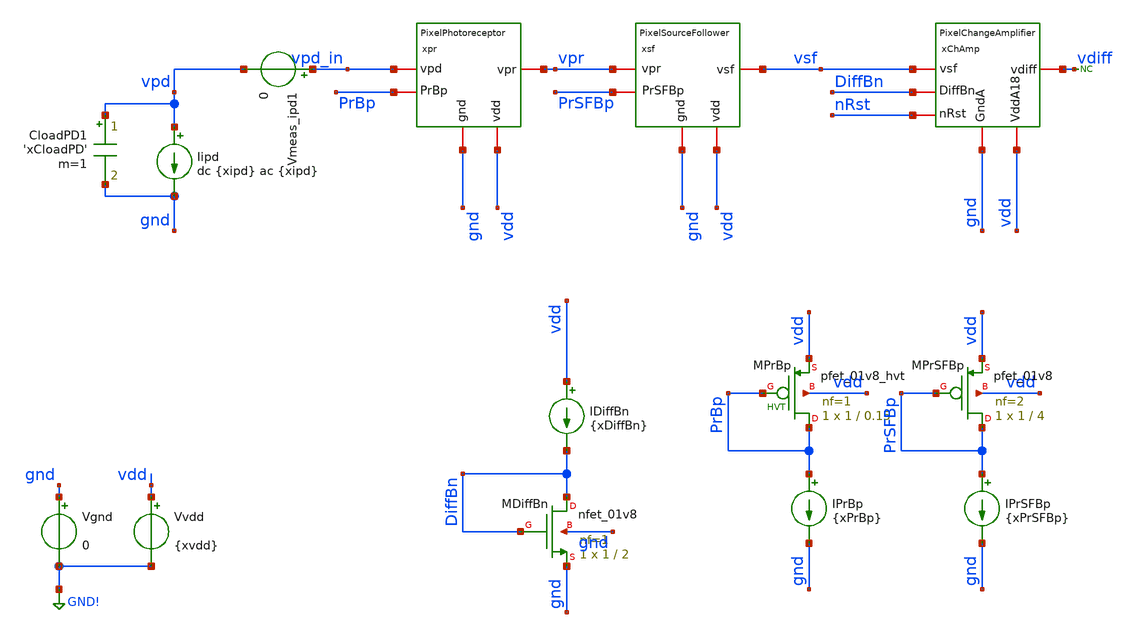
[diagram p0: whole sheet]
** sch_path: analog/klayout/production/final_merge_20260923/testbenches/cace/analog/xschem/tb_PixelGain_ac.sch
**.subckt tb_PixelGain_ac
Vgnd gnd GND! 0
Vvdd vdd GND! {xvdd}
xpr vdd PrBp gnd vpd_in vpr PixelPhotoreceptor
xsf vdd PrSFBp gnd vpr vsf PixelSourceFollower
Iipd vpd gnd dc {xipd} ac {xipd}
CloadPD1 vpd gnd 'xCloadPD' m=1
Vmeas_ipd1 vpd_in vpd 0
xChAmp vdd DiffBn gnd vsf vdiff nRst PixelChangeAmplifier
XMDiffBn DiffBn DiffBn gnd gnd sky130_fd_pr__nfet_01v8 L=2 W=1 nf=1 ad='int((1 + 1)/2) * 1 / 1 * 0.29'
+ as='int((1 + 2)/2) * 1 / 1 * 0.29' pd='2*int((1 + 1)/2) * (1 / 1 + 0.29)' ps='2*int((1 + 2)/2) * (1 / 1 + 0.29)'
+ nrd='0.29 / 1 ' nrs='0.29 / 1 ' sa=0 sb=0 sd=0 mult=1 m=1
IDiffBn vdd DiffBn {xDiffBn}
IPrBp PrBp gnd {xPrBp}
XMPrBp PrBp PrBp vdd vdd sky130_fd_pr__pfet_01v8_hvt L=0.15 W=1 nf=1 ad='int((1 + 1)/2) * 1 / 1 * 0.29'
+ as='int((1 + 2)/2) * 1 / 1 * 0.29' pd='2*int((1 + 1)/2) * (1 / 1 + 0.29)' ps='2*int((1 + 2)/2) * (1 / 1 + 0.29)'
+ nrd='0.29 / 1 ' nrs='0.29 / 1 ' sa=0 sb=0 sd=0 mult=1 m=1
IPrSFBp PrSFBp gnd {xPrSFBp}
XMPrSFBp PrSFBp PrSFBp vdd vdd sky130_fd_pr__pfet_01v8 L=4 W=1 nf=2 ad='int((2 + 1)/2) * 1 / 2 * 0.29'
+ as='int((2 + 2)/2) * 1 / 2 * 0.29' pd='2*int((2 + 1)/2) * (1 / 2 + 0.29)' ps='2*int((2 + 2)/2) * (1 / 2 + 0.29)'
+ nrd='0.29 / 1 ' nrs='0.29 / 1 ' sa=0 sb=0 sd=0 mult=1 m=1
* noconn vdiff
**** begin user architecture code

** opencircuitdesign pdks install
.lib $::SKYWATER_MODELS/sky130.lib.spice tt



.temp 27

.option gmin=1e-16 abstol=1e-15 vntol=1e-9 reltol=1e-4 chgtol=1e-16
.option itl1=500 itl2=200
.option gminsteps=200 srcsteps=200

.param xvdd = 1.8
.param xipd = 1p
.param xPrBp = 10n
.param xPrSFBp = 100p
.param xDiffBn = 5n
.param xCloadPD = 30f

** nRst at vdd for normal operation (Mrst OFF)
VnRst nRst gnd {xvdd}

** Large inductor: DC short (sets OP) but AC open (no effect on freq response)
** Provides DC path for floating cap node xchamp.vd through vdiff
Lbias vdiff xchamp.vd 1000T

.save all

.control
** OP with nRst=vdd, .nodeset guides floating nodes
op
let vd_op = v(xchamp.vd)
let vdiff_op = v(vdiff)
echo
echo '=== OP (nRst=vdd) ==='
echo '    vd    =' $&vd_op 'V'
echo '    vdiff =' $&vdiff_op 'V'
write tb_PixelGain_ac_op.raw

** AC sweep from this operating point
ac dec 50 1m 1G
write tb_PixelGain_ac.raw

echo
echo '=== AC analysis complete, running post-processing ==='
shell python3
+ /home/rpgraca/research/projects/telluride/2025/nic_eventcam/nic2025_openDVS/analog/xschem/process_PixelGain_ac.py tb_PixelGain_ac.raw
.endc


**** end user architecture code
**.ends

* expanding   symbol:  PixelPhotoreceptor.sym # of pins=5
** sym_path: analog/xschem/PixelPhotoreceptor.sym
** sch_path: analog/xschem/PixelPhotoreceptor.sch
.subckt PixelPhotoreceptor vdd PrBp gnd vpd vpr
*.iopin PrBp
*.iopin vdd
*.iopin vpd
*.iopin gnd
*.iopin vpr
XMpd vdd vpr vpd gnd sky130_fd_pr__nfet_01v8 L=0.3 W=0.42 nf=1 ad='int((1 + 1)/2) * 0.42 / 1 * 0.29'
+ as='int((1 + 2)/2) * 0.42 / 1 * 0.29' pd='2*int((1 + 1)/2) * (0.42 / 1 + 0.29)' ps='2*int((1 + 2)/2) * (0.42 / 1 + 0.29)'
+ nrd='0.29 / 0.42 ' nrs='0.29 / 0.42 ' sa=0 sb=0 sd=0 mult=1 m=1
XMpr_amp vpr vpd gnd gnd sky130_fd_pr__nfet_01v8 L=0.3 W=0.42 nf=1 ad='int((1 + 1)/2) * 0.42 / 1 * 0.29'
+ as='int((1 + 2)/2) * 0.42 / 1 * 0.29' pd='2*int((1 + 1)/2) * (0.42 / 1 + 0.29)' ps='2*int((1 + 2)/2) * (0.42 / 1 + 0.29)'
+ nrd='0.29 / 0.42 ' nrs='0.29 / 0.42 ' sa=0 sb=0 sd=0 mult=1 m=1
XMprBias vpr PrBp vdd vdd sky130_fd_pr__pfet_01v8_hvt L=0.15 W=0.5 nf=1 ad='int((1 + 1)/2) * 0.5 / 1 * 0.29'
+ as='int((1 + 2)/2) * 0.5 / 1 * 0.29' pd='2*int((1 + 1)/2) * (0.5 / 1 + 0.29)' ps='2*int((1 + 2)/2) * (0.5 / 1 + 0.29)'
+ nrd='0.29 / 0.5 ' nrs='0.29 / 0.5 ' sa=0 sb=0 sd=0 mult=1 m=1
.ends


* expanding   symbol:  PixelSourceFollower.sym # of pins=5
** sym_path: analog/xschem/PixelSourceFollower.sym
** sch_path: analog/xschem/PixelSourceFollower.sch
.subckt PixelSourceFollower vdd PrSFBp gnd vpr vsf
*.iopin gnd
*.iopin PrSFBp
*.iopin vpr
*.iopin vsf
*.iopin vdd
XMsfBias vsf PrSFBp vdd vdd sky130_fd_pr__pfet_01v8 L=1.6 W=0.42 nf=1 ad='int((1 + 1)/2) * 0.42 / 1 * 0.29'
+ as='int((1 + 2)/2) * 0.42 / 1 * 0.29' pd='2*int((1 + 1)/2) * (0.42 / 1 + 0.29)' ps='2*int((1 + 2)/2) * (0.42 / 1 + 0.29)'
+ nrd='0.29 / 0.42 ' nrs='0.29 / 0.42 ' sa=0 sb=0 sd=0 mult=1 m=1
XMsf gnd vpr vsf vdd sky130_fd_pr__pfet_01v8 L=0.25 W=0.42 nf=1 ad='int((1 + 1)/2) * 0.42 / 1 * 0.29'
+ as='int((1 + 2)/2) * 0.42 / 1 * 0.29' pd='2*int((1 + 1)/2) * (0.42 / 1 + 0.29)' ps='2*int((1 + 2)/2) * (0.42 / 1 + 0.29)'
+ nrd='0.29 / 0.42 ' nrs='0.29 / 0.42 ' sa=0 sb=0 sd=0 mult=1 m=1
.ends


* expanding   symbol:  PixelChangeAmplifier.sym # of pins=6
** sym_path: analog/xschem/PixelChangeAmplifier.sym
** sch_path: analog/xschem/PixelChangeAmplifier.sch
.subckt PixelChangeAmplifier VddA18 DiffBn GndA vsf vdiff nRst
*.iopin DiffBn
*.iopin vsf
*.iopin VddA18
*.iopin GndA
*.iopin vdiff
*.iopin nRst
XC1b vd vsf sky130_fd_pr__cap_mim_m3_1 W=6.47 L=1.505 MF=1 m=1
XC2 vd vdiff sky130_fd_pr__cap_mim_m3_1 W=1 L=1 MF=1 m=1
XMchAmpBias vdiff DiffBn GndA GndA sky130_fd_pr__nfet_01v8 L=1.5 W=1.5 nf=1 ad='int((1 + 1)/2) * 1.5 / 1 * 0.29'
+ as='int((1 + 2)/2) * 1.5 / 1 * 0.29' pd='2*int((1 + 1)/2) * (1.5 / 1 + 0.29)' ps='2*int((1 + 2)/2) * (1.5 / 1 + 0.29)'
+ nrd='0.29 / 1.5 ' nrs='0.29 / 1.5 ' sa=0 sb=0 sd=0 mult=1 m=1
XMrst vdiff nRst vd VddA18 sky130_fd_pr__pfet_01v8_hvt L=0.42 W=0.42 nf=1 ad='int((1 + 1)/2) * 0.42 / 1 * 0.29'
+ as='int((1 + 2)/2) * 0.42 / 1 * 0.29' pd='2*int((1 + 1)/2) * (0.42 / 1 + 0.29)' ps='2*int((1 + 2)/2) * (0.42 / 1 + 0.29)'
+ nrd='0.29 / 0.42 ' nrs='0.29 / 0.42 ' sa=0 sb=0 sd=0 mult=1 m=1
XMchAmp vdiff vd VddA18 VddA18 sky130_fd_pr__pfet_01v8 L=1.5 W=1.5 nf=1 ad='int((1 + 1)/2) * 1.5 / 1 * 0.29'
+ as='int((1 + 2)/2) * 1.5 / 1 * 0.29' pd='2*int((1 + 1)/2) * (1.5 / 1 + 0.29)' ps='2*int((1 + 2)/2) * (1.5 / 1 + 0.29)'
+ nrd='0.29 / 1.5 ' nrs='0.29 / 1.5 ' sa=0 sb=0 sd=0 mult=1 m=1
XC1a vd vsf sky130_fd_pr__cap_mim_m3_1 W=2.27 L=3.985 MF=1 m=1
.ends

.GLOBAL GND!
.end
